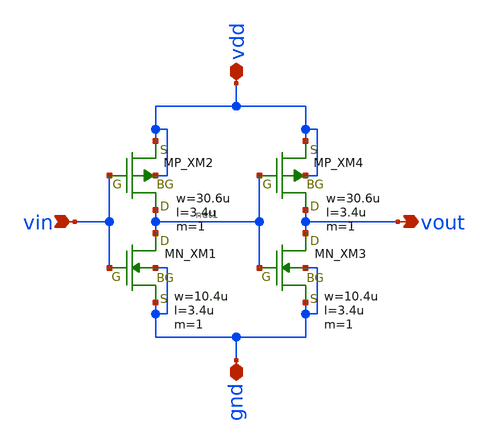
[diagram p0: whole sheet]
** sch_path: member_project/ringOSC/noritsuna/buffer.sch
**.subckt buffer vdd vin vout gnd
*.iopin vdd
*.ipin vin
*.opin vout
*.iopin gnd
XM1 net1 vin gnd gnd NMOS w=10.4u l=3.4u as=0 ad=0 ps=0 pd=0 nrd=0 nrs=0 m=1
XM2 net1 vin vdd vdd PMOS w=30.6u l=3.4u as=0 ad=0 ps=0 pd=0 nrd=0 nrs=0 m=1
XM3 vout net1 gnd gnd NMOS w=10.4u l=3.4u as=0 ad=0 ps=0 pd=0 nrd=0 nrs=0 m=1
XM4 vout net1 vdd vdd PMOS w=30.6u l=3.4u as=0 ad=0 ps=0 pd=0 nrd=0 nrs=0 m=1
**.ends
.end
